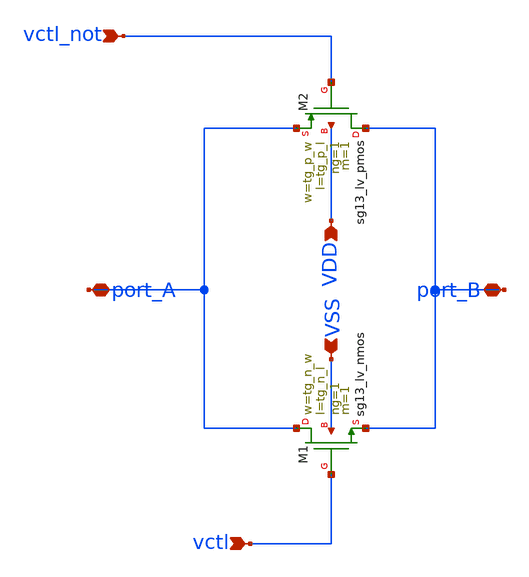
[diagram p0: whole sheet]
** sch_path: analog-db/drawings/shared/transmission_gate_pair.sch
* Copyright 2026 MacAnalog Research Group
**.subckt transmission_gate_pair port_A port_B vctl VSS VDD vctl_not
*.iopin port_A
*.iopin port_B
*.ipin vctl
*.ipin VSS
*.ipin VDD
*.ipin vctl_not
XM1 port_A vctl port_B VSS sg13_lv_nmos w=tg_n_w l=tg_n_l ng=1 m=1 mm_ok=1
XM2 port_B vctl_not port_A VDD sg13_lv_pmos w=tg_p_w l=tg_p_l ng=1 m=1 mm_ok=1
**.ends
.end
